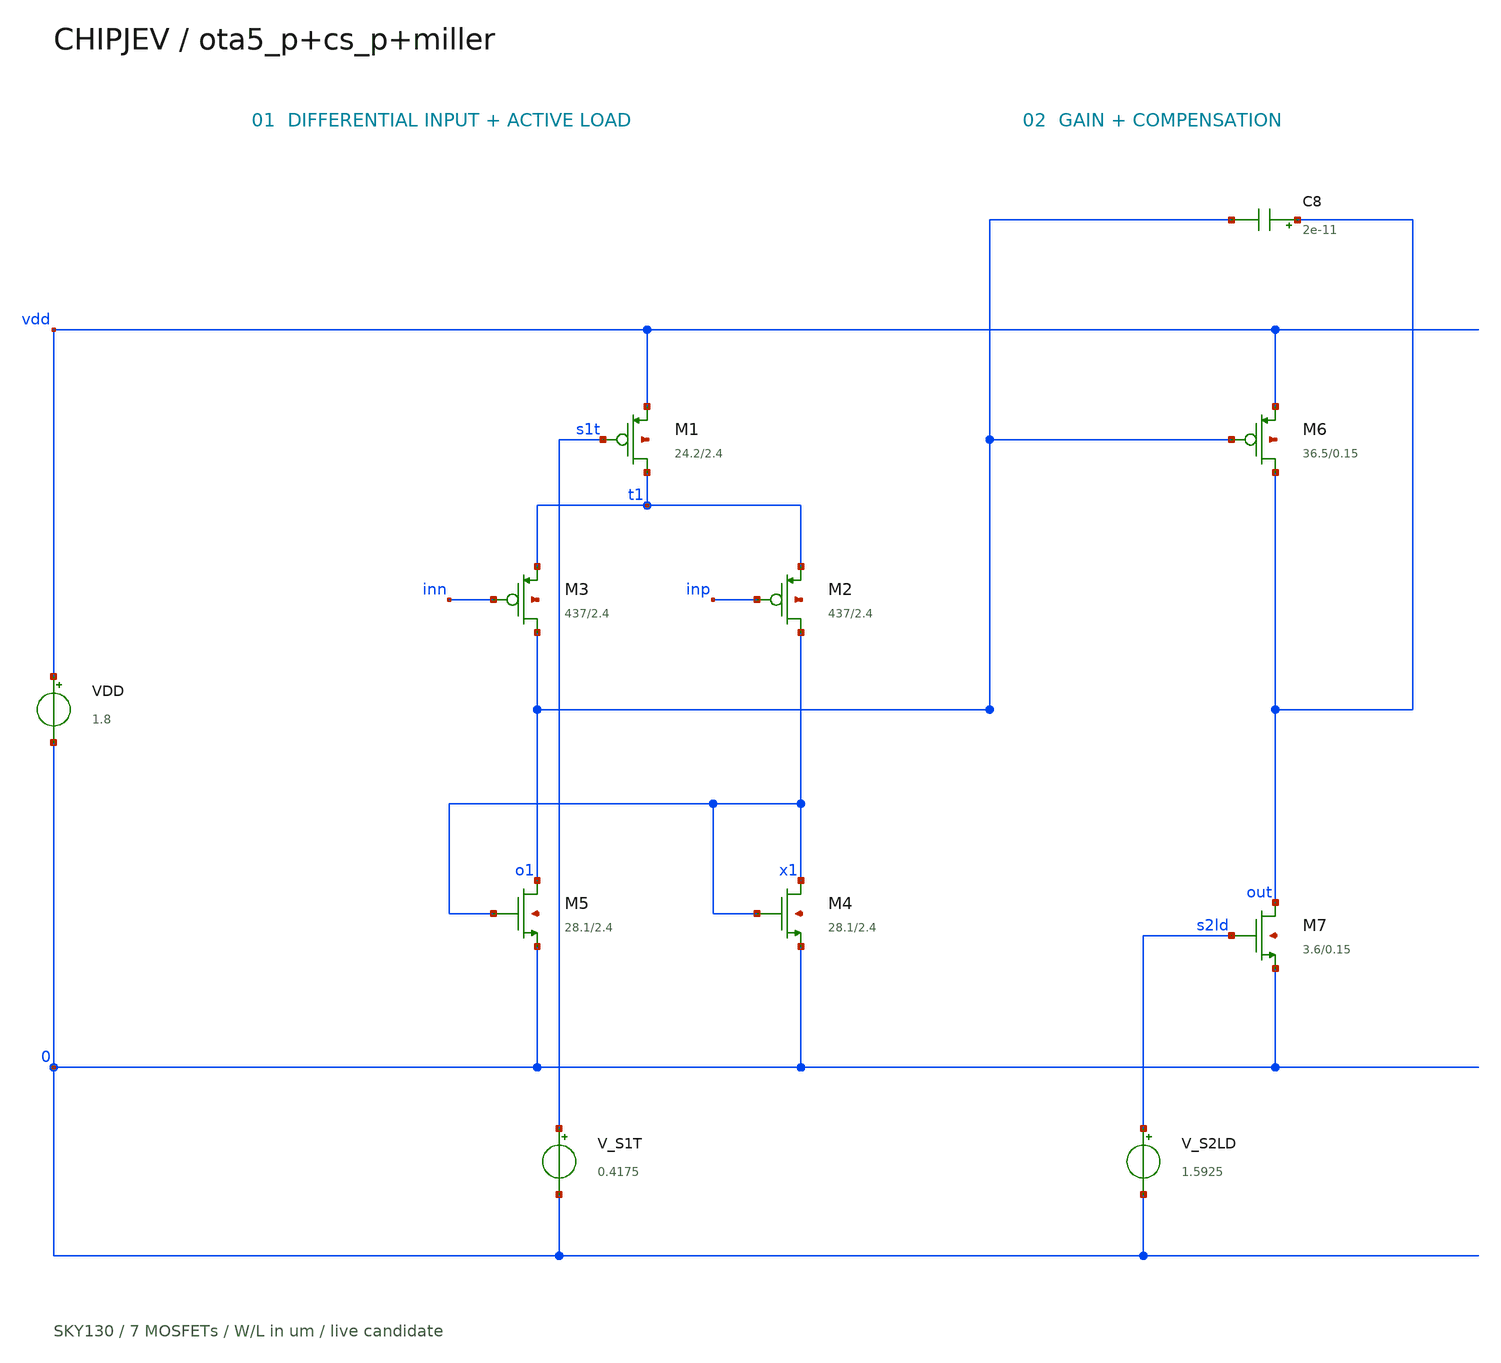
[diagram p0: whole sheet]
** sch_path: experiments/analog-layout/opamp-speed/circuit.sch
**.subckt circuit
VDD vdd 0 1.8
XM1 t1 s1t vdd vdd sky130_fd_pr__pfet_01v8 L=2.4 W=24.24 nf=1 ad=7.0296 as=7.0296 pd=49.06 ps=49.06
+ nrd=0.0119637 nrs=0.0119637 sa=0 sb=0 sd=0 mult=1 m=1
XM2 x1 inp t1 vdd sky130_fd_pr__pfet_01v8 L=2.4 W=436.77 nf=9 ad=70.3685 as=70.3685 pd=488.2
+ ps=488.2 nrd=0.000663965 nrs=0.000663965 sa=0 sb=0 sd=0 mult=1 m=1
XM3 o1 inn t1 vdd sky130_fd_pr__pfet_01v8 L=2.4 W=436.77 nf=9 ad=70.3685 as=70.3685 pd=488.2
+ ps=488.2 nrd=0.000663965 nrs=0.000663965 sa=0 sb=0 sd=0 mult=1 m=1
XM4 x1 x1 0 0 sky130_fd_pr__nfet_01v8 L=2.4 W=28.08 nf=1 ad=8.1432 as=8.1432 pd=56.74 ps=56.74
+ nrd=0.0103276 nrs=0.0103276 sa=0 sb=0 sd=0 mult=1 m=1
XM5 o1 x1 0 0 sky130_fd_pr__nfet_01v8 L=2.4 W=28.08 nf=1 ad=8.1432 as=8.1432 pd=56.74 ps=56.74
+ nrd=0.0103276 nrs=0.0103276 sa=0 sb=0 sd=0 mult=1 m=1
XM6 out o1 vdd vdd sky130_fd_pr__pfet_01v8 L=0.15 W=36.45 nf=1 ad=10.5705 as=10.5705 pd=73.48
+ ps=73.48 nrd=0.0079561 nrs=0.0079561 sa=0 sb=0 sd=0 mult=1 m=1
XM7 out s2ld 0 0 sky130_fd_pr__nfet_01v8 L=0.15 W=3.6 nf=1 ad=1.044 as=1.044 pd=7.78 ps=7.78
+ nrd=0.0805556 nrs=0.0805556 sa=0 sb=0 sd=0 mult=1 m=1
C8 out o1 2e-11 m=1
V_S1T s1t 0 0.4175
V_S2LD s2ld 0 1.5925
**.ends
.end
